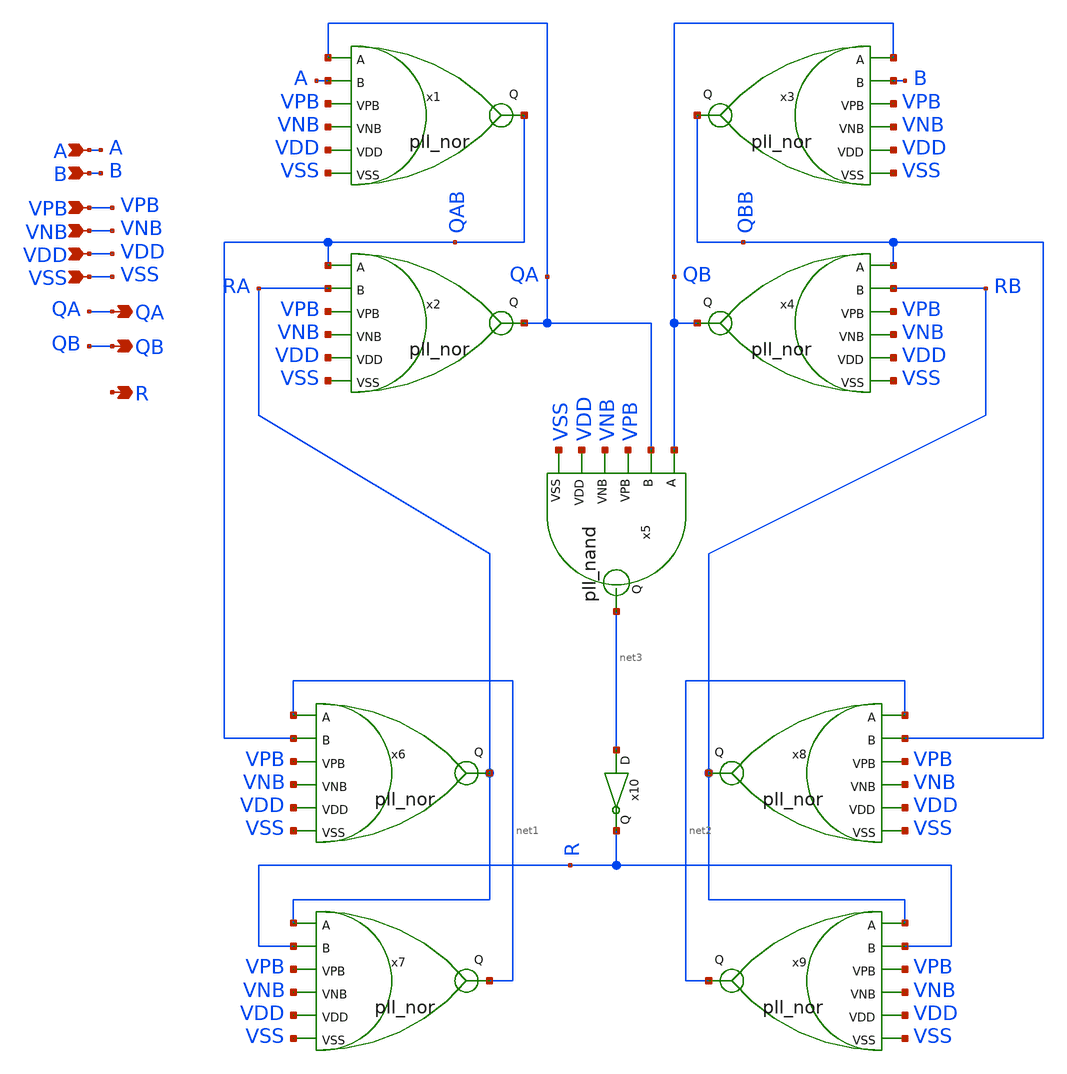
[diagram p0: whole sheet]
** sch_path: xschem/pll_pfd.sch
**.subckt pll_pfd A B VDD VPB VNB VSS QA QB R
*.ipin A
*.ipin B
*.ipin VDD
*.ipin VPB
*.ipin VNB
*.ipin VSS
*.opin QA
*.opin QB
*.opin R
x1 QA A VPB VNB VDD QAB VSS pll_nor
x2 QAB RA VPB VNB VDD QA VSS pll_nor
x5 QB QA VPB VNB VDD VSS net3 pll_nand
x3 QB B VPB VNB VDD QBB VSS pll_nor
x4 QBB RB VPB VNB VDD QB VSS pll_nor
x6 net1 QAB VPB VNB VDD RA VSS pll_nor
x7 RA R VPB VNB VDD net1 VSS pll_nor
x8 net2 QBB VPB VNB VDD RB VSS pll_nor
x9 RB R VPB VNB VDD net2 VSS pll_nor
x10 net3 R VDD VSS pll_inv1
**.ends

* expanding   symbol:  pll_nor.sym # of pins=7
** sym_path: xschem/pll_nor.sym
** sch_path: xschem/pll_nor.sch
.subckt pll_nor A B VPB VNB VDD Q VSS
*.opin Q
*.ipin A
*.ipin B
*.ipin VDD
*.ipin VPB
*.ipin VNB
*.ipin VSS
XM3 net1 A net2 VPB sky130_fd_pr__pfet_01v8_lvt L=0.35 W=1 nf=1 ad='int((nf+1)/2) * W/nf * 0.29' as='int((nf+2)/2) * W/nf * 0.29'
+ pd='2*int((nf+1)/2) * (W/nf + 0.29)' ps='2*int((nf+2)/2) * (W/nf + 0.29)' nrd='0.29 / W' nrs='0.29 / W'
+ sa=0 sb=0 sd=0 mult=1 m=1
vpwr VDD net2 0
.save i(vpwr)
XM1 Q A VSS VNB sky130_fd_pr__nfet_01v8_lvt L=0.25 W=0.5 nf=1 ad='int((nf+1)/2) * W/nf * 0.29' as='int((nf+2)/2) * W/nf * 0.29'
+ pd='2*int((nf+1)/2) * (W/nf + 0.29)' ps='2*int((nf+2)/2) * (W/nf + 0.29)' nrd='0.29 / W' nrs='0.29 / W'
+ sa=0 sb=0 sd=0 mult=1 m=1
XM2 Q B net1 VPB sky130_fd_pr__pfet_01v8_lvt L=0.35 W=1 nf=1 ad='int((nf+1)/2) * W/nf * 0.29' as='int((nf+2)/2) * W/nf * 0.29'
+ pd='2*int((nf+1)/2) * (W/nf + 0.29)' ps='2*int((nf+2)/2) * (W/nf + 0.29)' nrd='0.29 / W' nrs='0.29 / W'
+ sa=0 sb=0 sd=0 mult=1 m=1
XM4 Q B VSS VNB sky130_fd_pr__nfet_01v8_lvt L=0.25 W=0.5 nf=1 ad='int((nf+1)/2) * W/nf * 0.29' as='int((nf+2)/2) * W/nf * 0.29'
+ pd='2*int((nf+1)/2) * (W/nf + 0.29)' ps='2*int((nf+2)/2) * (W/nf + 0.29)' nrd='0.29 / W' nrs='0.29 / W'
+ sa=0 sb=0 sd=0 mult=1 m=1
.ends


* expanding   symbol:  pll_nand.sym # of pins=7
** sym_path: xschem/pll_nand.sym
** sch_path: xschem/pll_nand.sch
.subckt pll_nand A B VPB VNB VDD VSS Q
*.opin Q
*.ipin A
*.ipin B
*.ipin VDD
*.ipin VPB
*.ipin VNB
*.ipin VSS
XM3 Q B net2 VPB sky130_fd_pr__pfet_01v8_lvt L=0.35 W=1 nf=1 ad='int((nf+1)/2) * W/nf * 0.29' as='int((nf+2)/2) * W/nf * 0.29'
+ pd='2*int((nf+1)/2) * (W/nf + 0.29)' ps='2*int((nf+2)/2) * (W/nf + 0.29)' nrd='0.29 / W' nrs='0.29 / W'
+ sa=0 sb=0 sd=0 mult=1 m=1
vpwr VDD net2 0
.save i(vpwr)
XM1 net1 B VSS VNB sky130_fd_pr__nfet_01v8_lvt L=0.25 W=0.5 nf=1 ad='int((nf+1)/2) * W/nf * 0.29' as='int((nf+2)/2) * W/nf * 0.29'
+ pd='2*int((nf+1)/2) * (W/nf + 0.29)' ps='2*int((nf+2)/2) * (W/nf + 0.29)' nrd='0.29 / W' nrs='0.29 / W'
+ sa=0 sb=0 sd=0 mult=1 m=1
XM2 Q A net2 VPB sky130_fd_pr__pfet_01v8_lvt L=0.35 W=1 nf=1 ad='int((nf+1)/2) * W/nf * 0.29' as='int((nf+2)/2) * W/nf * 0.29'
+ pd='2*int((nf+1)/2) * (W/nf + 0.29)' ps='2*int((nf+2)/2) * (W/nf + 0.29)' nrd='0.29 / W' nrs='0.29 / W'
+ sa=0 sb=0 sd=0 mult=1 m=1
XM4 Q A net1 VNB sky130_fd_pr__nfet_01v8_lvt L=0.25 W=0.5 nf=1 ad='int((nf+1)/2) * W/nf * 0.29' as='int((nf+2)/2) * W/nf * 0.29'
+ pd='2*int((nf+1)/2) * (W/nf + 0.29)' ps='2*int((nf+2)/2) * (W/nf + 0.29)' nrd='0.29 / W' nrs='0.29 / W'
+ sa=0 sb=0 sd=0 mult=1 m=1
.ends


* expanding   symbol:  pll_inv1.sym # of pins=2
** sym_path: xschem/pll_inv1.sym
** sch_path: xschem/pll_inv1.sch
.subckt pll_inv1 D Q VDD VSS
*.opin Q
*.ipin D
*.ipin VDD
*.ipin VSS
XM3 Q D net1 net1 sky130_fd_pr__pfet_01v8_lvt L=0.5 W=1 nf=1 ad='int((nf+1)/2) * W/nf * 0.29' as='int((nf+2)/2) * W/nf * 0.29'
+ pd='2*int((nf+1)/2) * (W/nf + 0.29)' ps='2*int((nf+2)/2) * (W/nf + 0.29)' nrd='0.29 / W' nrs='0.29 / W'
+ sa=0 sb=0 sd=0 mult=1 m=1
vpwr VDD net1 0
.save i(vpwr)
XM1 Q D VSS VSS sky130_fd_pr__nfet_01v8_lvt L=0.25 W=0.5 nf=1 ad='int((nf+1)/2) * W/nf * 0.29' as='int((nf+2)/2) * W/nf * 0.29'
+ pd='2*int((nf+1)/2) * (W/nf + 0.29)' ps='2*int((nf+2)/2) * (W/nf + 0.29)' nrd='0.29 / W' nrs='0.29 / W'
+ sa=0 sb=0 sd=0 mult=1 m=1
.ends

.end
